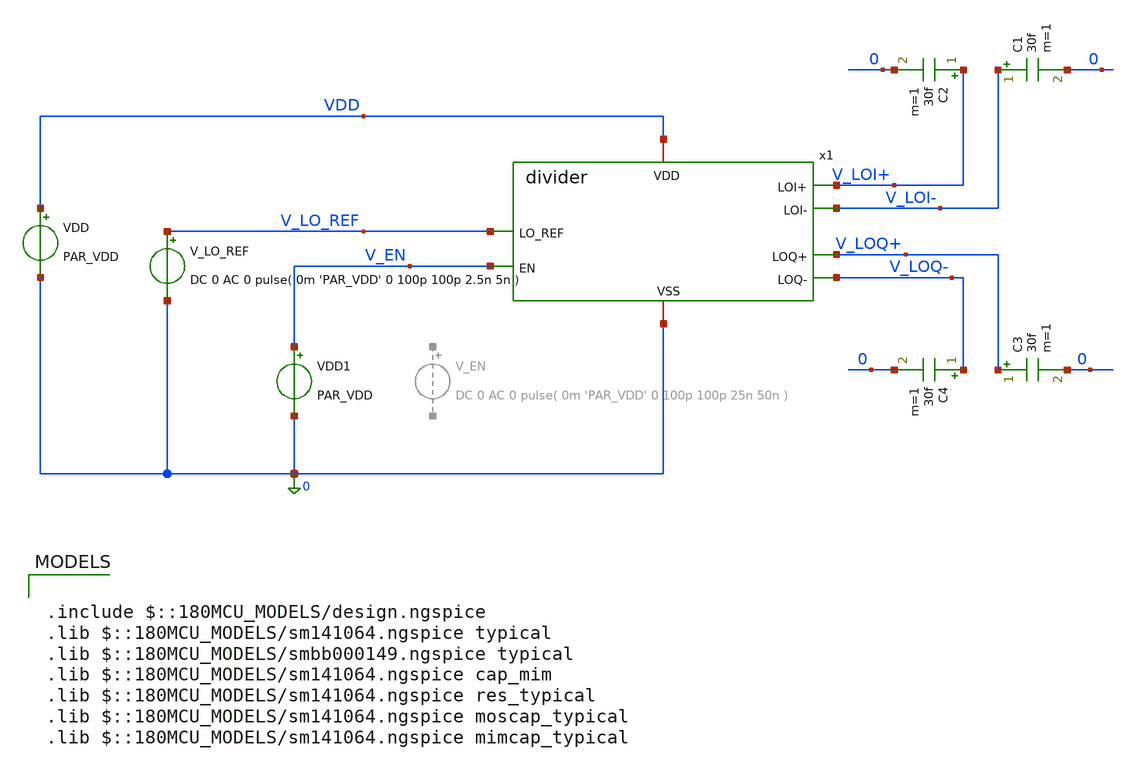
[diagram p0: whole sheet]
** sch_path: designs/divider/testbench/tb_divider.sch
**.subckt tb_divider
VDD VDD 0 PAR_VDD
V_LO_REF V_LO_REF 0 DC 0 AC 0 pulse( 0m 'PAR_VDD' 0 100p 100p 2.5n 5n )
x1 VDD 0 V_LO_REF V_LOI+ V_LOI- V_LOQ+ V_LOQ- V_EN divider
C1 V_LOI- 0 30f m=1
C2 V_LOI+ 0 30f m=1
C3 V_LOQ+ 0 30f m=1
C4 V_LOQ- 0 30f m=1
VDD1 V_EN 0 PAR_VDD
**** begin user architecture code

.include $::180MCU_MODELS/design.ngspice
.lib $::180MCU_MODELS/sm141064.ngspice typical
.lib $::180MCU_MODELS/smbb000149.ngspice typical
.lib $::180MCU_MODELS/sm141064.ngspice cap_mim
.lib $::180MCU_MODELS/sm141064.ngspice res_typical
.lib $::180MCU_MODELS/sm141064.ngspice moscap_typical
.lib $::180MCU_MODELS/sm141064.ngspice mimcap_typical



** PARAMS

.PARAM PAR_VDD=3.3

.control
destroy all
save all
write tb_divider.raw
wrdata /foss/designs/Divider_design/tb_divider.txt

op
print v(V_LOI+) v(V_LOI-)


;transient analysis
tran 0.01ns 10us


plot v(V_LO_REF) v(x1.LOI+_INTERNAL) v(x1.LOI-_INTERNAL) v(x1.LOQ+_INTERNAL) v(x1.LOQ-_INTERNAL)
+ ;plot internal signals
plot v(V_LO_REF) v(V_LOI+)+3 v(V_LOI-)+3  v(V_LOQ+)-3 v(V_LOQ-)-3 ;plot divider output
plot v(V_LO_REF) v(V_LOI+)-v(V_LOI-) v(V_LOQ+)-v(V_LOQ-); plot differential output
;plot v(V_EN) v(x1.EN_BAR) v(x1.LO_REF_GATED) v(x1.LO_REF_BAR); plot enable signal and clock signal
+ status

plot i(vdd)*2.5 ;transient power

;plot i(v.x1.v1) plot i(v.x1.v2)
;plot v(V_LO_REF) v(x1.LO_REF_BAR)


;fft of input and output
;let V_LOI = v(V_LOI+,V_LOI-)
;let V_LOQ = v(V_LOQ+, V_LOQ-)
;let LO_REF_slice = v(V_LO_REF)[1000,9000] ; LO_REF transient output from t=10ns to t=100ns (0.01ns
+ resolution at index 100 to index 10000)
;let LOI_slice = v(V_LOI)[1000,9000];
;let LOQ_slice = v(V_LOQ)[1000,9000];
;linearize np=auto2n v(LO_REF_slice) v(LOI_slice) v(LOQ__slice)
;fft v(LO_REF_slice) v(LOI_slice) v(LOQ_slice)
;plot mag(LO_REF_slice) mag(LOI_slice) mag(LOQ_slice)



.endc


**** end user architecture code
**.ends
.end
